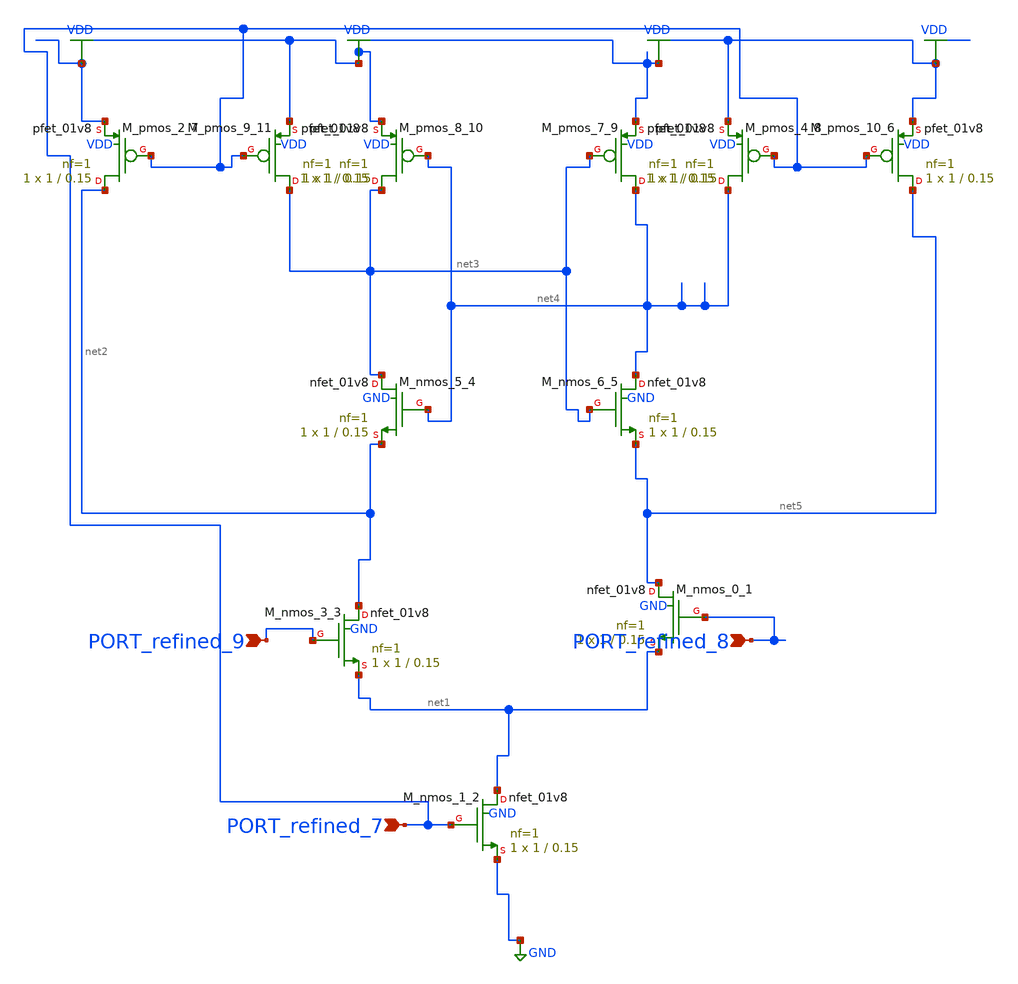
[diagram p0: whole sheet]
** sch_path: schematics/Image2Net/046.sch
**.subckt 046 PORT_refined_9 PORT_refined_8 PORT_refined_7
*.ipin PORT_refined_9
*.ipin PORT_refined_8
*.ipin PORT_refined_7
XM_nmos_0_1 net5 PORT_refined_8 net1 GND sky130_fd_pr__nfet_01v8 L=0.15 W=1 nf=1 ad='int((1 + 1)/2) * 1 / 1 * 0.29'
+ as='int((1 + 2)/2) * 1 / 1 * 0.29' pd='2*int((1 + 1)/2) * (1 / 1 + 0.29)' ps='2*int((1 + 2)/2) * (1 / 1 + 0.29)'
+ nrd='0.29 / 1 ' nrs='0.29 / 1 ' sa=0 sb=0 sd=0 mult=1 m=1
XM_nmos_1_2 net1 PORT_refined_7 GND GND sky130_fd_pr__nfet_01v8 L=0.15 W=1 nf=1 ad='int((1 + 1)/2) * 1 / 1 * 0.29'
+ as='int((1 + 2)/2) * 1 / 1 * 0.29' pd='2*int((1 + 1)/2) * (1 / 1 + 0.29)' ps='2*int((1 + 2)/2) * (1 / 1 + 0.29)'
+ nrd='0.29 / 1 ' nrs='0.29 / 1 ' sa=0 sb=0 sd=0 mult=1 m=1
XM_nmos_3_3 net2 PORT_refined_9 net1 GND sky130_fd_pr__nfet_01v8 L=0.15 W=1 nf=1 ad='int((1 + 1)/2) * 1 / 1 * 0.29'
+ as='int((1 + 2)/2) * 1 / 1 * 0.29' pd='2*int((1 + 1)/2) * (1 / 1 + 0.29)' ps='2*int((1 + 2)/2) * (1 / 1 + 0.29)'
+ nrd='0.29 / 1 ' nrs='0.29 / 1 ' sa=0 sb=0 sd=0 mult=1 m=1
XM_nmos_5_4 net3 net4 net2 GND sky130_fd_pr__nfet_01v8 L=0.15 W=1 nf=1 ad='int((1 + 1)/2) * 1 / 1 * 0.29'
+ as='int((1 + 2)/2) * 1 / 1 * 0.29' pd='2*int((1 + 1)/2) * (1 / 1 + 0.29)' ps='2*int((1 + 2)/2) * (1 / 1 + 0.29)'
+ nrd='0.29 / 1 ' nrs='0.29 / 1 ' sa=0 sb=0 sd=0 mult=1 m=1
XM_nmos_6_5 net4 net3 net5 GND sky130_fd_pr__nfet_01v8 L=0.15 W=1 nf=1 ad='int((1 + 1)/2) * 1 / 1 * 0.29'
+ as='int((1 + 2)/2) * 1 / 1 * 0.29' pd='2*int((1 + 1)/2) * (1 / 1 + 0.29)' ps='2*int((1 + 2)/2) * (1 / 1 + 0.29)'
+ nrd='0.29 / 1 ' nrs='0.29 / 1 ' sa=0 sb=0 sd=0 mult=1 m=1
XM_pmos_10_6 net5 PORT_refined_7 VDD VDD sky130_fd_pr__pfet_01v8 L=0.15 W=1 nf=1 ad='int((1 + 1)/2) * 1 / 1 * 0.29'
+ as='int((1 + 2)/2) * 1 / 1 * 0.29' pd='2*int((1 + 1)/2) * (1 / 1 + 0.29)' ps='2*int((1 + 2)/2) * (1 / 1 + 0.29)'
+ nrd='0.29 / 1 ' nrs='0.29 / 1 ' sa=0 sb=0 sd=0 mult=1 m=1
XM_pmos_2_7 net2 PORT_refined_7 VDD VDD sky130_fd_pr__pfet_01v8 L=0.15 W=1 nf=1 ad='int((1 + 1)/2) * 1 / 1 * 0.29'
+ as='int((1 + 2)/2) * 1 / 1 * 0.29' pd='2*int((1 + 1)/2) * (1 / 1 + 0.29)' ps='2*int((1 + 2)/2) * (1 / 1 + 0.29)'
+ nrd='0.29 / 1 ' nrs='0.29 / 1 ' sa=0 sb=0 sd=0 mult=1 m=1
XM_pmos_4_8 net4 PORT_refined_7 VDD VDD sky130_fd_pr__pfet_01v8 L=0.15 W=1 nf=1 ad='int((1 + 1)/2) * 1 / 1 * 0.29'
+ as='int((1 + 2)/2) * 1 / 1 * 0.29' pd='2*int((1 + 1)/2) * (1 / 1 + 0.29)' ps='2*int((1 + 2)/2) * (1 / 1 + 0.29)'
+ nrd='0.29 / 1 ' nrs='0.29 / 1 ' sa=0 sb=0 sd=0 mult=1 m=1
XM_pmos_7_9 net4 net3 VDD VDD sky130_fd_pr__pfet_01v8 L=0.15 W=1 nf=1 ad='int((1 + 1)/2) * 1 / 1 * 0.29'
+ as='int((1 + 2)/2) * 1 / 1 * 0.29' pd='2*int((1 + 1)/2) * (1 / 1 + 0.29)' ps='2*int((1 + 2)/2) * (1 / 1 + 0.29)'
+ nrd='0.29 / 1 ' nrs='0.29 / 1 ' sa=0 sb=0 sd=0 mult=1 m=1
XM_pmos_8_10 net3 net4 VDD VDD sky130_fd_pr__pfet_01v8 L=0.15 W=1 nf=1 ad='int((1 + 1)/2) * 1 / 1 * 0.29'
+ as='int((1 + 2)/2) * 1 / 1 * 0.29' pd='2*int((1 + 1)/2) * (1 / 1 + 0.29)' ps='2*int((1 + 2)/2) * (1 / 1 + 0.29)'
+ nrd='0.29 / 1 ' nrs='0.29 / 1 ' sa=0 sb=0 sd=0 mult=1 m=1
XM_pmos_9_11 net3 PORT_refined_7 VDD VDD sky130_fd_pr__pfet_01v8 L=0.15 W=1 nf=1 ad='int((1 + 1)/2) * 1 / 1 * 0.29'
+ as='int((1 + 2)/2) * 1 / 1 * 0.29' pd='2*int((1 + 1)/2) * (1 / 1 + 0.29)' ps='2*int((1 + 2)/2) * (1 / 1 + 0.29)'
+ nrd='0.29 / 1 ' nrs='0.29 / 1 ' sa=0 sb=0 sd=0 mult=1 m=1
**.ends
.GLOBAL GND
.GLOBAL VDD
.end
